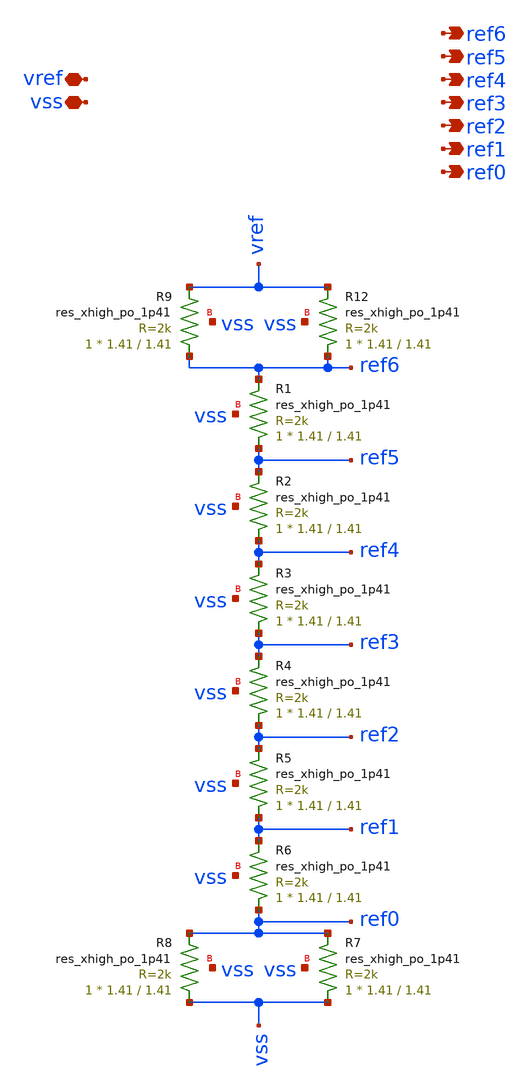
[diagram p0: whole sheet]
** sch_path: xsch/ip/res_ladder_vref/res_ladder_vref.sch
**.subckt res_ladder_vref vref vss ref0 ref1 ref2 ref3 ref4 ref5 ref6
*.iopin vref
*.iopin vss
*.opin ref0
*.opin ref1
*.opin ref2
*.opin ref3
*.opin ref4
*.opin ref5
*.opin ref6
XR12 ref6 vref vss sky130_fd_pr__res_xhigh_po_1p41 L=1.41 mult=1 m=1
XR1 ref5 ref6 vss sky130_fd_pr__res_xhigh_po_1p41 L=1.41 mult=1 m=1
XR2 ref4 ref5 vss sky130_fd_pr__res_xhigh_po_1p41 L=1.41 mult=1 m=1
XR3 ref3 ref4 vss sky130_fd_pr__res_xhigh_po_1p41 L=1.41 mult=1 m=1
XR4 ref2 ref3 vss sky130_fd_pr__res_xhigh_po_1p41 L=1.41 mult=1 m=1
XR5 ref1 ref2 vss sky130_fd_pr__res_xhigh_po_1p41 L=1.41 mult=1 m=1
XR6 ref0 ref1 vss sky130_fd_pr__res_xhigh_po_1p41 L=1.41 mult=1 m=1
XR7 vss ref0 vss sky130_fd_pr__res_xhigh_po_1p41 L=1.41 mult=1 m=1
XR8 vss ref0 vss sky130_fd_pr__res_xhigh_po_1p41 L=1.41 mult=1 m=1
XR9 ref6 vref vss sky130_fd_pr__res_xhigh_po_1p41 L=1.41 mult=1 m=1
**.ends
.end
